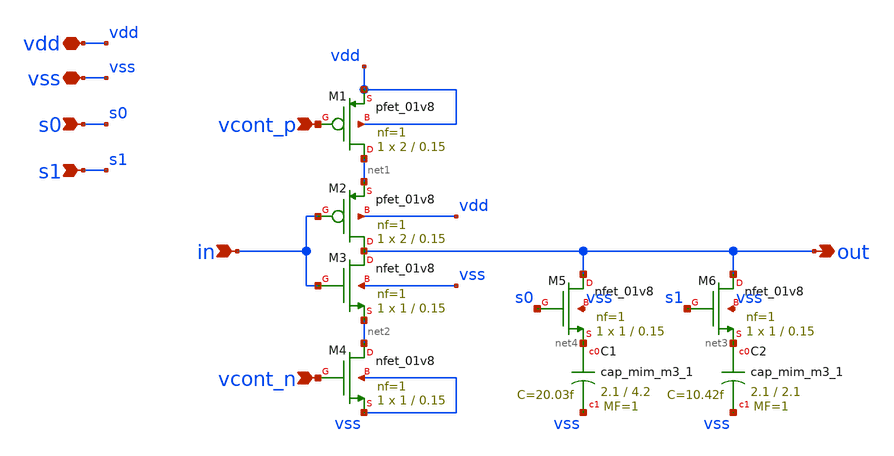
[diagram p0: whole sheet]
** sch_path: xschem/delay_stage.sch
**.subckt delay_stage in out vdd vcont_n vcont_p s0 s1 vss
*.ipin in
*.opin out
*.iopin vdd
*.ipin vcont_n
*.ipin vcont_p
*.ipin s0
*.ipin s1
*.iopin vss
XM3 out in net2 vss sky130_fd_pr__nfet_01v8 L=0.15 W=1 nf=1 ad='int((nf+1)/2) * W/nf * 0.29' as='int((nf+2)/2) * W/nf * 0.29'
+ pd='2*int((nf+1)/2) * (W/nf + 0.29)' ps='2*int((nf+2)/2) * (W/nf + 0.29)' nrd='0.29 / W' nrs='0.29 / W'
+ sa=0 sb=0 sd=0 mult=1 m=1
XM2 out in net1 vdd sky130_fd_pr__pfet_01v8 L=0.15 W=2 nf=1 ad='int((nf+1)/2) * W/nf * 0.29' as='int((nf+2)/2) * W/nf * 0.29'
+ pd='2*int((nf+1)/2) * (W/nf + 0.29)' ps='2*int((nf+2)/2) * (W/nf + 0.29)' nrd='0.29 / W' nrs='0.29 / W'
+ sa=0 sb=0 sd=0 mult=1 m=1
XM1 net1 vcont_p vdd vdd sky130_fd_pr__pfet_01v8 L=0.15 W=2 nf=1 ad='int((nf+1)/2) * W/nf * 0.29' as='int((nf+2)/2) * W/nf * 0.29'
+ pd='2*int((nf+1)/2) * (W/nf + 0.29)' ps='2*int((nf+2)/2) * (W/nf + 0.29)' nrd='0.29 / W' nrs='0.29 / W'
+ sa=0 sb=0 sd=0 mult=1 m=1
XM4 net2 vcont_n vss vss sky130_fd_pr__nfet_01v8 L=0.15 W=1 nf=1 ad='int((nf+1)/2) * W/nf * 0.29' as='int((nf+2)/2) * W/nf * 0.29'
+ pd='2*int((nf+1)/2) * (W/nf + 0.29)' ps='2*int((nf+2)/2) * (W/nf + 0.29)' nrd='0.29 / W' nrs='0.29 / W'
+ sa=0 sb=0 sd=0 mult=1 m=1
XC2 net3 vss sky130_fd_pr__cap_mim_m3_1 W=2.1 L=2.1 MF=1 m=1
XC1 net4 vss sky130_fd_pr__cap_mim_m3_1 W=2.1 L=4.2 MF=1 m=1
XM5 out s0 net4 vss sky130_fd_pr__nfet_01v8 L=0.15 W=1 nf=1 ad='int((nf+1)/2) * W/nf * 0.29' as='int((nf+2)/2) * W/nf * 0.29'
+ pd='2*int((nf+1)/2) * (W/nf + 0.29)' ps='2*int((nf+2)/2) * (W/nf + 0.29)' nrd='0.29 / W' nrs='0.29 / W'
+ sa=0 sb=0 sd=0 mult=1 m=1
XM6 out s1 net3 vss sky130_fd_pr__nfet_01v8 L=0.15 W=1 nf=1 ad='int((nf+1)/2) * W/nf * 0.29' as='int((nf+2)/2) * W/nf * 0.29'
+ pd='2*int((nf+1)/2) * (W/nf + 0.29)' ps='2*int((nf+2)/2) * (W/nf + 0.29)' nrd='0.29 / W' nrs='0.29 / W'
+ sa=0 sb=0 sd=0 mult=1 m=1
**.ends
.end
